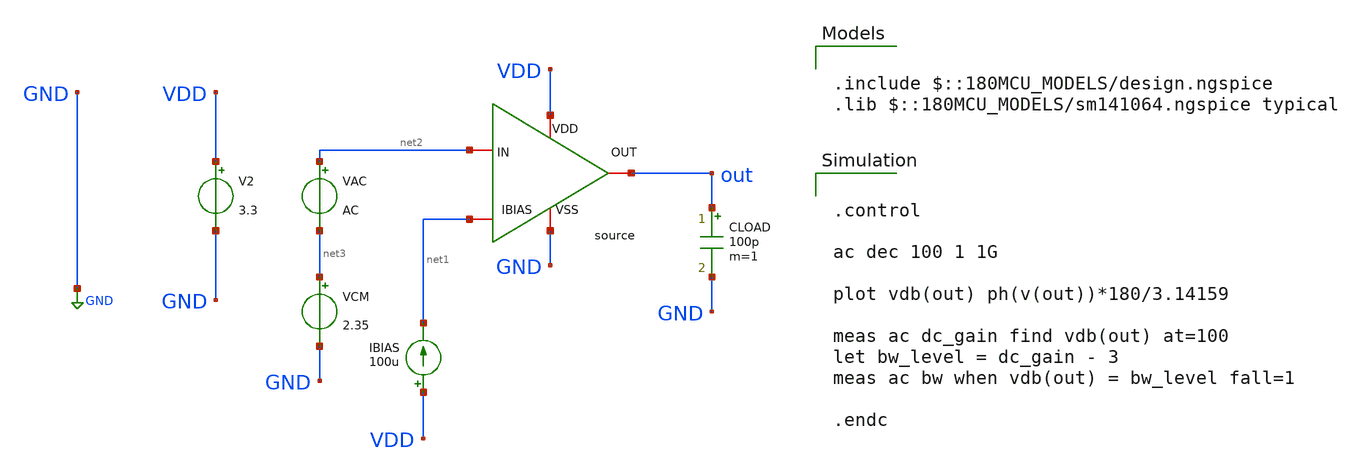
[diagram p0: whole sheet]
** sch_path: designs/libs/core_amps/cs_stage/tb/ac_tb.sch
**.subckt ac_tb
x1 VDD net2 net1 out GND cs_schematic
V2 VDD GND 3.3
IBIAS VDD net1 100u
CLOAD out GND 100p m=1
VCM net3 GND 2.35
VAC net2 net3 AC
**** begin user architecture code

.include $::180MCU_MODELS/design.ngspice
.lib $::180MCU_MODELS/sm141064.ngspice typical



.control

ac dec 100 1 1G

plot vdb(out) ph(v(out))*180/3.14159

meas ac dc_gain find vdb(out) at=100
let bw_level = dc_gain - 3
meas ac bw when vdb(out) = bw_level fall=1

.endc


**** end user architecture code
**.ends
.GLOBAL GND
.end
